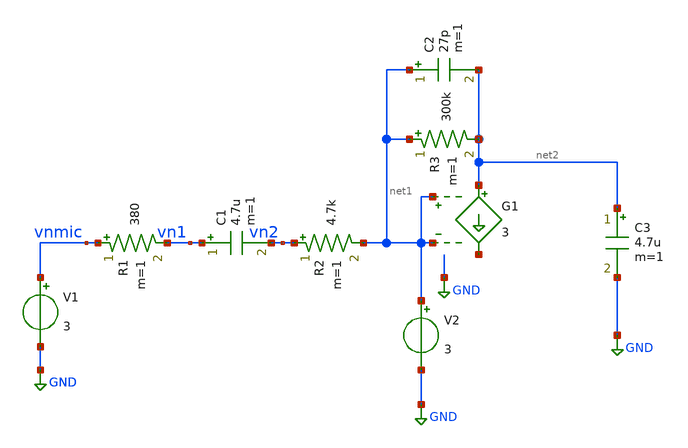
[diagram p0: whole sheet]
** sch_path: xschem/untitled.sch
**.subckt untitled
V1 vnmic GND 3
R1 vnmic vn1 380 m=1
C1 vn1 vn2 4.7u m=1
R2 vn2 net1 4.7k m=1
G1 net2 net3 net1 net1 3
R3 net1 net2 300k m=1
C2 net1 net2 27p m=1
V2 net1 GND 3
C3 net2 GND 4.7u m=1
**.ends
.GLOBAL GND
.end
